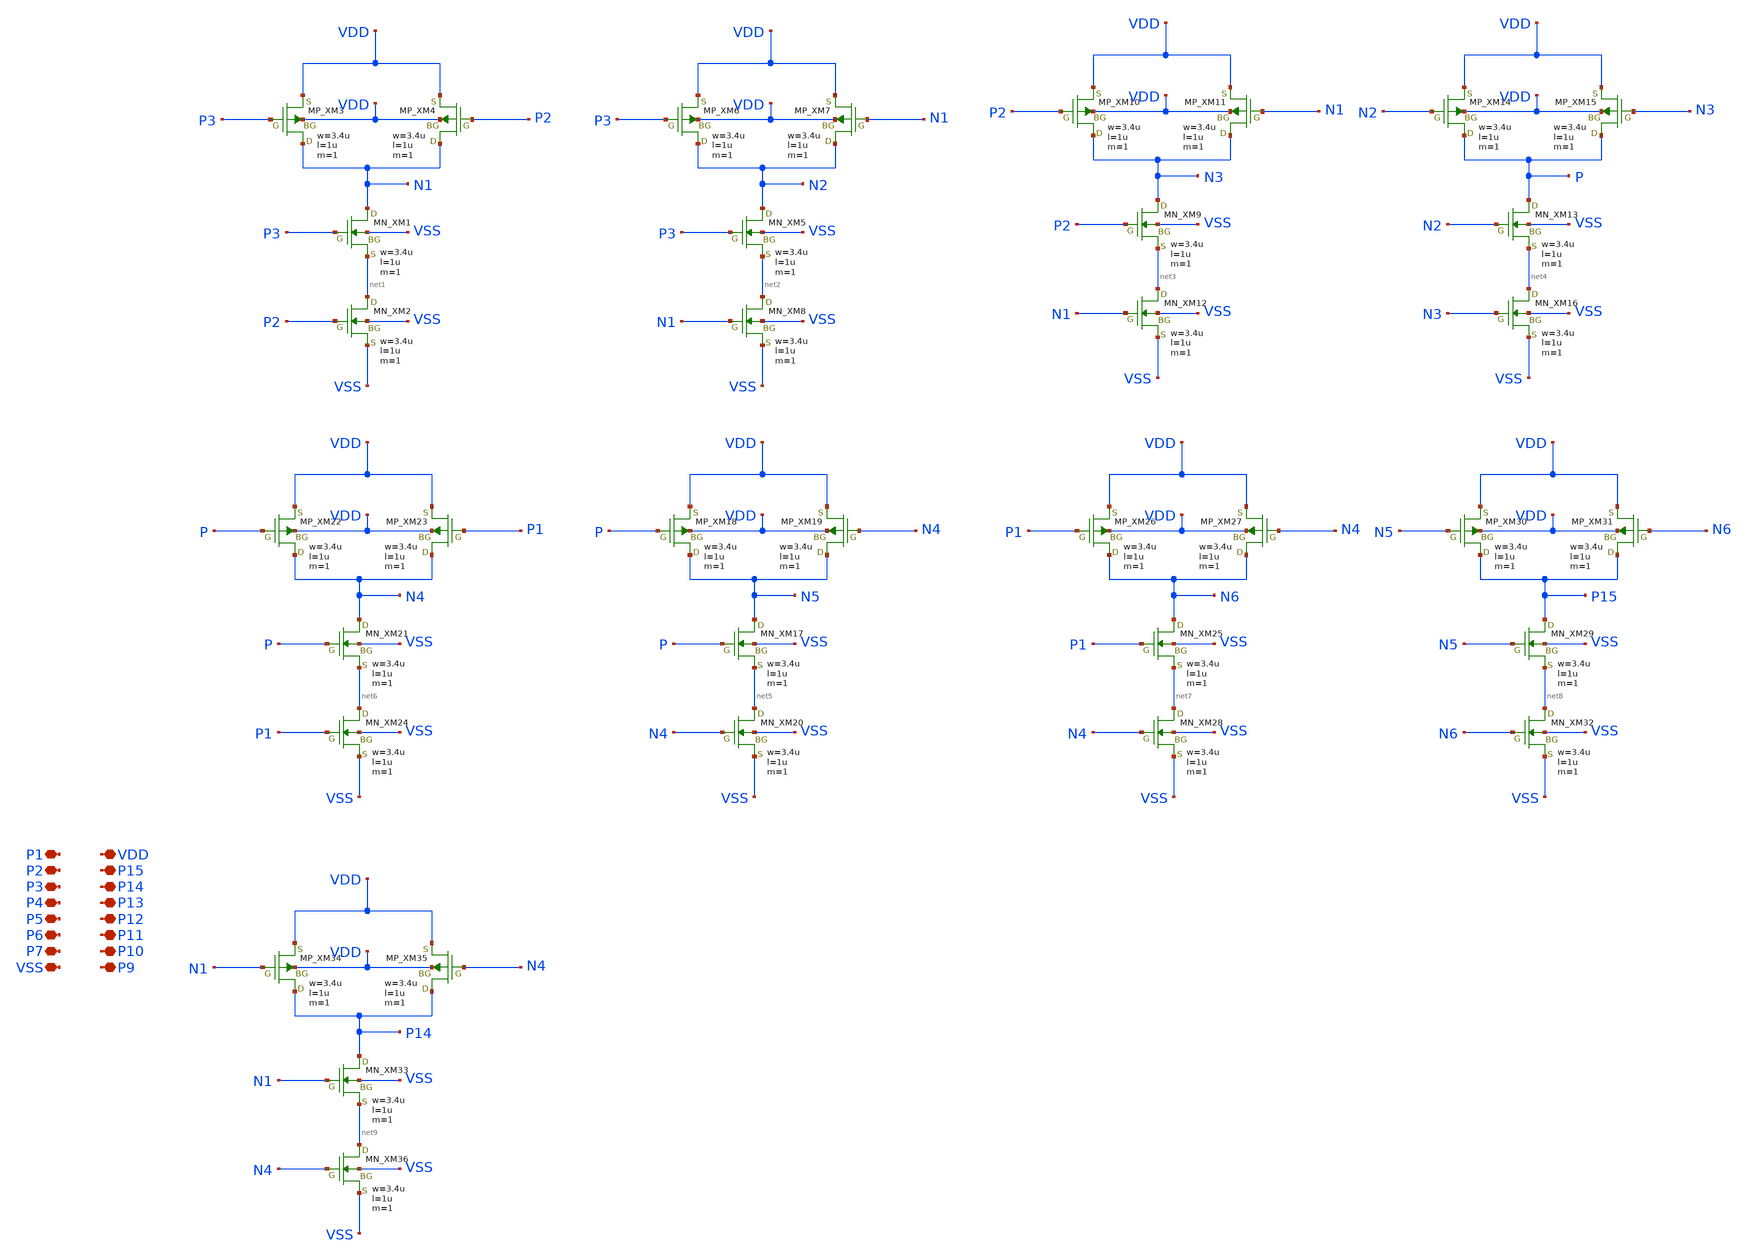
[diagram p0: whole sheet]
** sch_path: src/tr_1um_AriyoshiNaoki1016jp.sch
**.subckt tr_1um_AriyoshiNaoki1016jp P1 P2 P3 P4 P5 P6 P7 VSS VDD P15 P14 P13 P12 P11 P10 P9
*.iopin P1
*.iopin P2
*.iopin P3
*.iopin P4
*.iopin P5
*.iopin P6
*.iopin P7
*.iopin VSS
*.iopin VDD
*.iopin P15
*.iopin P14
*.iopin P13
*.iopin P12
*.iopin P11
*.iopin P10
*.iopin P9
XXM1 N1 P3 net1 VSS NMOS w=3.4u l=1u nrd=0 nrs=0 m=1
XXM3 N1 P3 VDD VDD PMOS w=3.4u l=1u nrd=0 nrs=0 m=1
XXM4 N1 P2 VDD VDD PMOS w=3.4u l=1u nrd=0 nrs=0 m=1
XXM2 net1 P2 VSS VSS NMOS w=3.4u l=1u nrd=0 nrs=0 m=1
XXM5 N2 P3 net2 VSS NMOS w=3.4u l=1u nrd=0 nrs=0 m=1
XXM6 N2 P3 VDD VDD PMOS w=3.4u l=1u nrd=0 nrs=0 m=1
XXM7 N2 N1 VDD VDD PMOS w=3.4u l=1u nrd=0 nrs=0 m=1
XXM8 net2 N1 VSS VSS NMOS w=3.4u l=1u nrd=0 nrs=0 m=1
XXM9 N3 P2 net3 VSS NMOS w=3.4u l=1u nrd=0 nrs=0 m=1
XXM10 N3 P2 VDD VDD PMOS w=3.4u l=1u nrd=0 nrs=0 m=1
XXM11 N3 N1 VDD VDD PMOS w=3.4u l=1u nrd=0 nrs=0 m=1
XXM12 net3 N1 VSS VSS NMOS w=3.4u l=1u nrd=0 nrs=0 m=1
XXM13 P N2 net4 VSS NMOS w=3.4u l=1u nrd=0 nrs=0 m=1
XXM14 P N2 VDD VDD PMOS w=3.4u l=1u nrd=0 nrs=0 m=1
XXM15 P N3 VDD VDD PMOS w=3.4u l=1u nrd=0 nrs=0 m=1
XXM16 net4 N3 VSS VSS NMOS w=3.4u l=1u nrd=0 nrs=0 m=1
XXM17 N5 P net5 VSS NMOS w=3.4u l=1u nrd=0 nrs=0 m=1
XXM18 N5 P VDD VDD PMOS w=3.4u l=1u nrd=0 nrs=0 m=1
XXM19 N5 N4 VDD VDD PMOS w=3.4u l=1u nrd=0 nrs=0 m=1
XXM20 net5 N4 VSS VSS NMOS w=3.4u l=1u nrd=0 nrs=0 m=1
XXM21 N4 P net6 VSS NMOS w=3.4u l=1u nrd=0 nrs=0 m=1
XXM22 N4 P VDD VDD PMOS w=3.4u l=1u nrd=0 nrs=0 m=1
XXM23 N4 P1 VDD VDD PMOS w=3.4u l=1u nrd=0 nrs=0 m=1
XXM24 net6 P1 VSS VSS NMOS w=3.4u l=1u nrd=0 nrs=0 m=1
XXM25 N6 P1 net7 VSS NMOS w=3.4u l=1u nrd=0 nrs=0 m=1
XXM26 N6 P1 VDD VDD PMOS w=3.4u l=1u nrd=0 nrs=0 m=1
XXM27 N6 N4 VDD VDD PMOS w=3.4u l=1u nrd=0 nrs=0 m=1
XXM28 net7 N4 VSS VSS NMOS w=3.4u l=1u nrd=0 nrs=0 m=1
XXM29 P15 N5 net8 VSS NMOS w=3.4u l=1u nrd=0 nrs=0 m=1
XXM30 P15 N5 VDD VDD PMOS w=3.4u l=1u nrd=0 nrs=0 m=1
XXM31 P15 N6 VDD VDD PMOS w=3.4u l=1u nrd=0 nrs=0 m=1
XXM32 net8 N6 VSS VSS NMOS w=3.4u l=1u nrd=0 nrs=0 m=1
XXM33 P14 N1 net9 VSS NMOS w=3.4u l=1u nrd=0 nrs=0 m=1
XXM34 P14 N1 VDD VDD PMOS w=3.4u l=1u nrd=0 nrs=0 m=1
XXM35 P14 N4 VDD VDD PMOS w=3.4u l=1u nrd=0 nrs=0 m=1
XXM36 net9 N4 VSS VSS NMOS w=3.4u l=1u nrd=0 nrs=0 m=1
**** begin user architecture code
 .include $::LIB/ip62_models
**** end user architecture code
**.ends
.end
